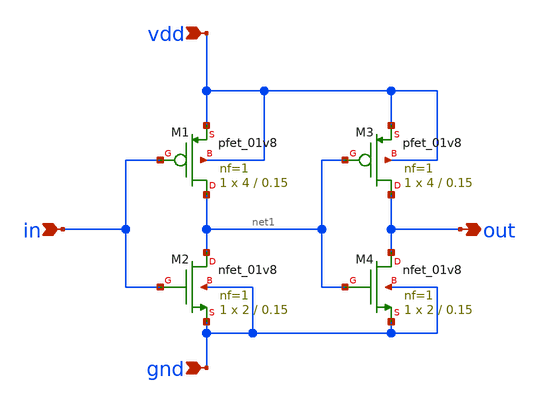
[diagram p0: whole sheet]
** sch_path: vcro/schem/buffer.sch
**.subckt buffer in gnd vdd out
*.ipin in
*.ipin gnd
*.ipin vdd
*.opin out
XM1 net1 in vdd vdd sky130_fd_pr__pfet_01v8 L=0.15 W=4 nf=1 ad='int((1 + 1)/2) * 4 / 1 * 0.29' as='int((1 + 2)/2) * 4 / 1 * 0.29'
+ pd='2*int((1 + 1)/2) * (4 / 1 + 0.29)' ps='2*int((1 + 2)/2) * (4 / 1 + 0.29)' nrd='0.29 / 4 ' nrs='0.29 / 4 '
+ sa=0 sb=0 sd=0 mult=1 m=1
XM2 net1 in gnd gnd sky130_fd_pr__nfet_01v8 L=0.15 W=2 nf=1 ad='int((1 + 1)/2) * 2 / 1 * 0.29' as='int((1 + 2)/2) * 2 / 1 * 0.29'
+ pd='2*int((1 + 1)/2) * (2 / 1 + 0.29)' ps='2*int((1 + 2)/2) * (2 / 1 + 0.29)' nrd='0.29 / 2 ' nrs='0.29 / 2 '
+ sa=0 sb=0 sd=0 mult=1 m=1
XM3 out net1 vdd vdd sky130_fd_pr__pfet_01v8 L=0.15 W=4 nf=1 ad='int((1 + 1)/2) * 4 / 1 * 0.29' as='int((1 + 2)/2) * 4 / 1 * 0.29'
+ pd='2*int((1 + 1)/2) * (4 / 1 + 0.29)' ps='2*int((1 + 2)/2) * (4 / 1 + 0.29)' nrd='0.29 / 4 ' nrs='0.29 / 4 '
+ sa=0 sb=0 sd=0 mult=1 m=1
XM4 out net1 gnd gnd sky130_fd_pr__nfet_01v8 L=0.15 W=2 nf=1 ad='int((1 + 1)/2) * 2 / 1 * 0.29' as='int((1 + 2)/2) * 2 / 1 * 0.29'
+ pd='2*int((1 + 1)/2) * (2 / 1 + 0.29)' ps='2*int((1 + 2)/2) * (2 / 1 + 0.29)' nrd='0.29 / 2 ' nrs='0.29 / 2 '
+ sa=0 sb=0 sd=0 mult=1 m=1
**.ends
.end
